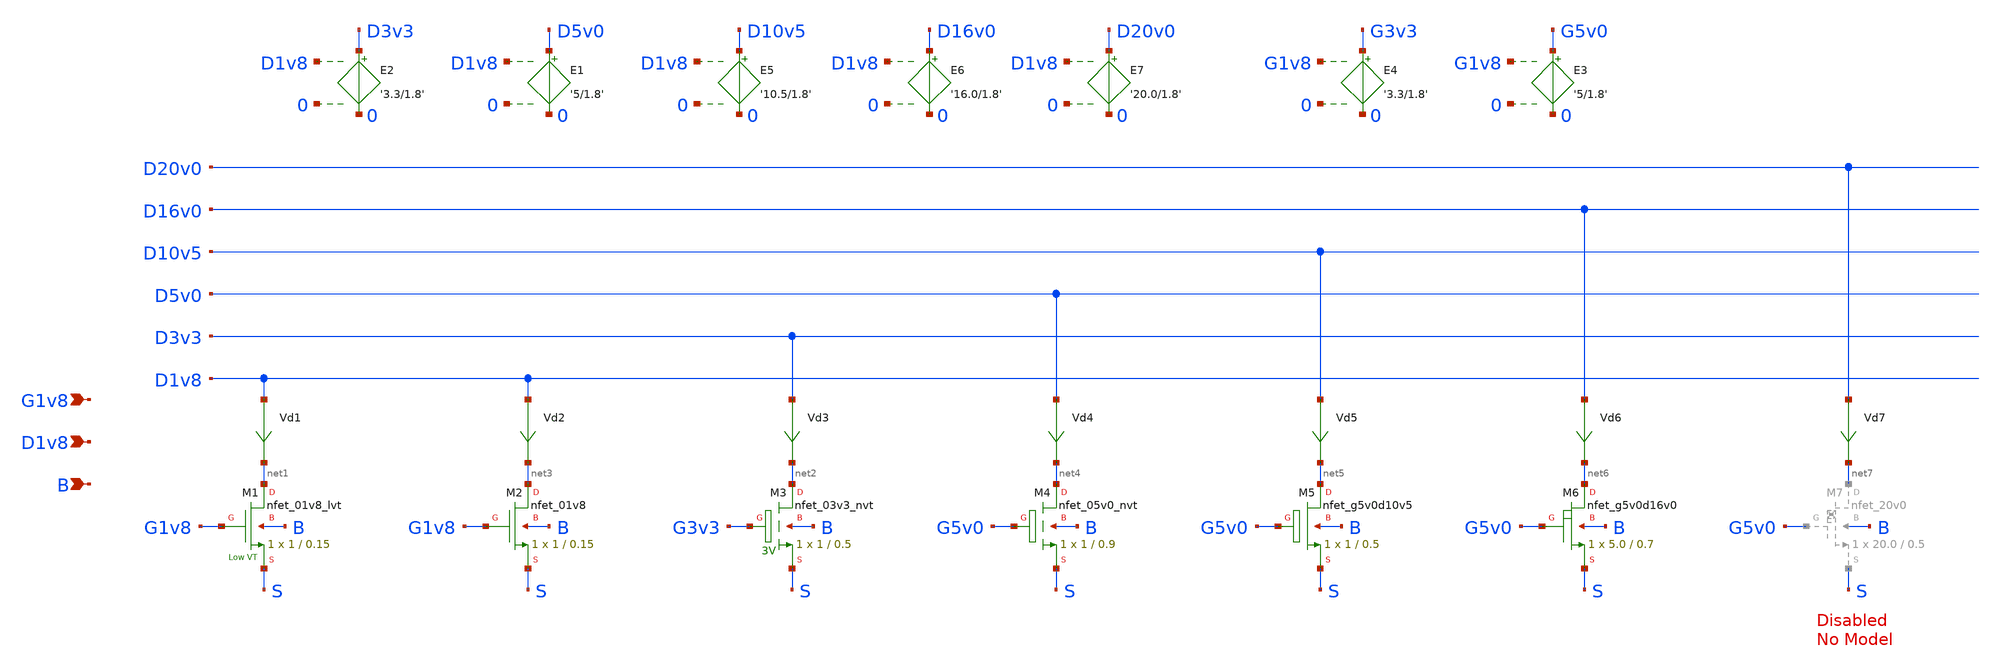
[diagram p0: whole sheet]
** sch_path: sky130_tests/test_nmos.sch
**.subckt test_nmos G1v8 D1v8 B
*.ipin G1v8
*.ipin D1v8
*.ipin B
Vd1 D1v8 net1 0
.save i(vd1)
Vd3 D3v3 net2 0
.save i(vd3)
XM1 net1 G1v8 S B sky130_fd_pr__nfet_01v8_lvt W=1 L=0.15 ad='W * 0.29' pd='W + 2 * 0.29' as='W * 0.29'
+ ps='W + 2 * 0.29' nrd=0 nrs=0 sa=0 sb=0 sd=0 nf=1 mult=1
XM2 net3 G1v8 S B sky130_fd_pr__nfet_01v8 W=1 L=0.15 ad='W * 0.29' pd='W + 2 * 0.29' as='W * 0.29' ps='W + 2 * 0.29'
+ nrd=0 nrs=0 sa=0 sb=0 sd=0 nf=1 mult=1
Vd2 D1v8 net3 0
.save i(vd2)
XM3 net2 G3v3 S B sky130_fd_pr__nfet_03v3_nvt W=1 L=0.5 ad='W * 0.29' pd='W + 2 * 0.29' as='W * 0.29'
+ ps='W + 2 * 0.29' nrd=0 nrs=0 sa=0 sb=0 sd=0 nf=1 mult=1
Vd4 D5v0 net4 0
.save i(vd4)
XM4 net4 G5v0 S B sky130_fd_pr__nfet_05v0_nvt W=1 L=0.9 ad='W * 0.29' pd='W + 2 * 0.29' as='W * 0.29'
+ ps='W + 2 * 0.29' nrd=0 nrs=0 sa=0 sb=0 sd=0 nf=1 mult=1
E1 D5v0 0 D1v8 0 '5/1.8'
E2 D3v3 0 D1v8 0 '3.3/1.8'
E3 G5v0 0 G1v8 0 '5/1.8'
E4 G3v3 0 G1v8 0 '3.3/1.8'
Vd5 D10v5 net5 0
.save i(vd5)
E5 D10v5 0 D1v8 0 '10.5/1.8'
XM5 net5 G5v0 S B sky130_fd_pr__nfet_g5v0d10v5 W=1 L=0.5 ad='W * 0.29' pd='W + 2 * 0.29' as='W * 0.29'
+ ps='W + 2 * 0.29' nrd=0 nrs=0 sa=0 sb=0 sd=0 nf=1 mult=1
E6 D16v0 0 D1v8 0 '16.0/1.8'
Vd6 D16v0 net6 0
.save i(vd6)
XM6 net6 G5v0 S B sky130_fd_pr__nfet_g5v0d16v0 W=5.0 L=0.7 ad='W * 0.29' pd='W + 2 * 0.29' as='W * 0.29'
+ ps='W + 2 * 0.29' nrd=0 nrs=0 sa=0 sb=0 sd=0 nf=1 mult=1
Vd7 D20v0 net7 0
.save i(vd7)
E7 D20v0 0 D1v8 0 '20.0/1.8'
**** begin user architecture code

.lib "/home/schippes/sky130_fd_pr/models/sky130.lib.spice" tt
** contains only tt corner, loads faster
* .lib "/home/schippes/sky130_fd_pr/models/sky130.lib_stefan_tt.spice" tt

* temporary fix: some model equations use temp instead of the true
* ngspice temperature variable, 'temper'
.param temp=27

vg G1v8 0 0
vs s 0 0
vd D1v8 0 0
vb b 0 0
.control
dc vd 0 1.8 0.01 vg 0 1.8 0.2
* plot all.vd1#branch vs D1v8
* plot all.vd2#branch vs D1v8
* plot all.vd3#branch vs D3v3
plot all.vd4#branch vs D5v0
plot all.vd5#branch vs D10v5
plot all.vd6#branch vs D16v0
plot all.vd7#branch vs D20v0
.endc


**** end user architecture code
**.ends
.end
